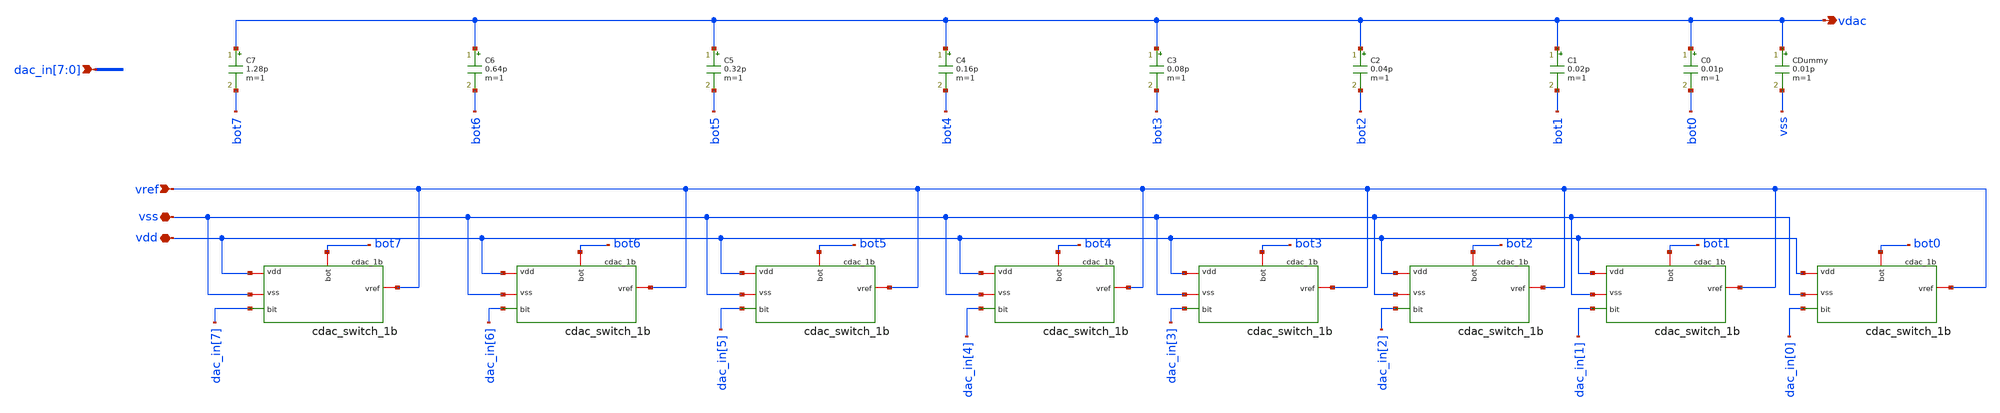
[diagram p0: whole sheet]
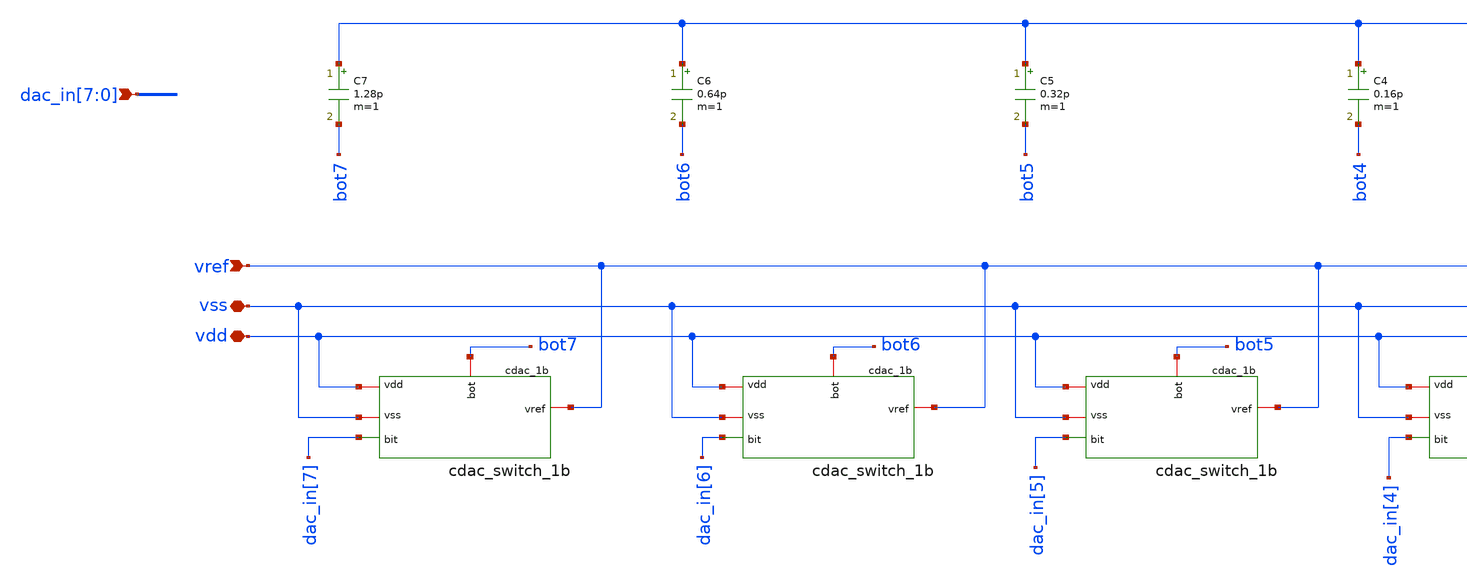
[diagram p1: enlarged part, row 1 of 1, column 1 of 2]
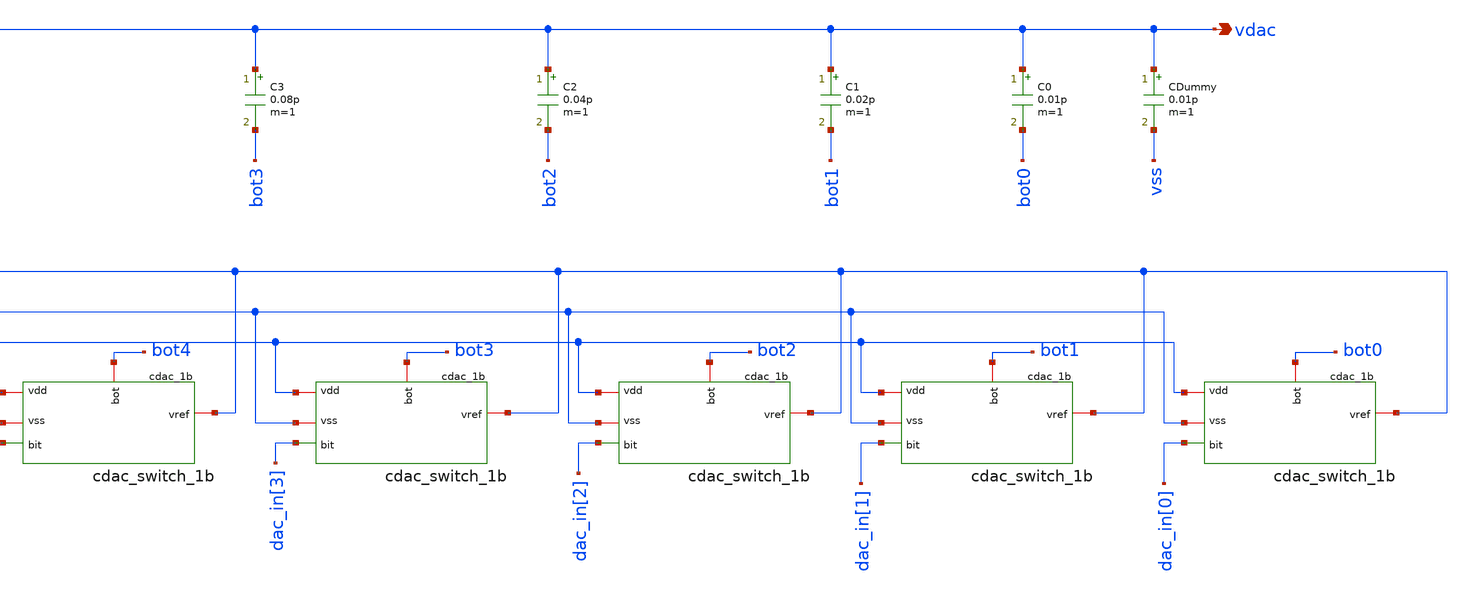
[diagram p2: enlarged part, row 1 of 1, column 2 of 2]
** sch_path: xschem/sar_adc/blocks/cdac/cdac_8bit.sch
**.subckt cdac_8bit vref vdd vss vdac
*+ dac_in[7],dac_in[6],dac_in[5],dac_in[4],dac_in[3],dac_in[2],dac_in[1],dac_in[0]
*.ipin vref
*.iopin vdd
*.iopin vss
*.opin vdac
*.ipin dac_in[7],dac_in[6],dac_in[5],dac_in[4],dac_in[3],dac_in[2],dac_in[1],dac_in[0]
C0 vdac bot0 0.01p m=1
C1 vdac bot1 0.02p m=1
C2 vdac bot2 0.04p m=1
C3 vdac bot3 0.08p m=1
C4 vdac bot4 0.16p m=1
C5 vdac bot5 0.32p m=1
C6 vdac bot6 0.64p m=1
C7 vdac bot7 1.28p m=1
XSW0 vref vdd vss bot0 dac_in[0] cdac_switch_1b
XSW1 vref vdd vss bot1 dac_in[1] cdac_switch_1b
XSW2 vref vdd vss bot2 dac_in[2] cdac_switch_1b
XSW3 vref vdd vss bot3 dac_in[3] cdac_switch_1b
XSW4 vref vdd vss bot4 dac_in[4] cdac_switch_1b
XSW5 vref vdd vss bot5 dac_in[5] cdac_switch_1b
XSW6 vref vdd vss bot6 dac_in[6] cdac_switch_1b
XSW7 vref vdd vss bot7 dac_in[7] cdac_switch_1b
CDummy vdac vss 0.01p m=1
**.ends

* expanding   symbol:  sar_adc/blocks/cdac/cdac_switch_1b.sym # of pins=5
** sym_path: xschem/sar_adc/blocks/cdac/cdac_switch_1b.sym
** sch_path: xschem/sar_adc/blocks/cdac/cdac_switch_1b.sch
.subckt cdac_switch_1b vref vdd vss bot bit
*.iopin vdd
*.iopin vss
*.iopin vref
*.ipin bit
*.iopin bot
XM1 bit_b bit vdd vdd pfet_03v3 L=0.28u W=1u nf=1 ad='int((nf+1)/2) * W/nf * 0.18u' as='int((nf+2)/2) * W/nf * 0.18u'
+ pd='2*int((nf+1)/2) * (W/nf + 0.18u)' ps='2*int((nf+2)/2) * (W/nf + 0.18u)' nrd='0.18u / W' nrs='0.18u / W'
+ sa=0 sb=0 sd=0 m=1
XM2 bit_b bit vss vss nfet_03v3 L=0.28u W=0.5u nf=1 ad='int((nf+1)/2) * W/nf * 0.18u' as='int((nf+2)/2) * W/nf * 0.18u'
+ pd='2*int((nf+1)/2) * (W/nf + 0.18u)' ps='2*int((nf+2)/2) * (W/nf + 0.18u)' nrd='0.18u / W' nrs='0.18u / W'
+ sa=0 sb=0 sd=0 m=1
XM3 bot bit_b vref vdd pfet_03v3 L=0.28u W=4u nf=1 ad='int((nf+1)/2) * W/nf * 0.18u' as='int((nf+2)/2) * W/nf * 0.18u'
+ pd='2*int((nf+1)/2) * (W/nf + 0.18u)' ps='2*int((nf+2)/2) * (W/nf + 0.18u)' nrd='0.18u / W' nrs='0.18u / W'
+ sa=0 sb=0 sd=0 m=1
XM4 vref bit bot vss nfet_03v3 L=0.28u W=2u nf=1 ad='int((nf+1)/2) * W/nf * 0.18u' as='int((nf+2)/2) * W/nf * 0.18u'
+ pd='2*int((nf+1)/2) * (W/nf + 0.18u)' ps='2*int((nf+2)/2) * (W/nf + 0.18u)' nrd='0.18u / W' nrs='0.18u / W'
+ sa=0 sb=0 sd=0 m=1
XM5 bot bit vss vdd pfet_03v3 L=0.28u W=4u nf=1 ad='int((nf+1)/2) * W/nf * 0.18u' as='int((nf+2)/2) * W/nf * 0.18u'
+ pd='2*int((nf+1)/2) * (W/nf + 0.18u)' ps='2*int((nf+2)/2) * (W/nf + 0.18u)' nrd='0.18u / W' nrs='0.18u / W'
+ sa=0 sb=0 sd=0 m=1
XM6 vss bit_b bot vss nfet_03v3 L=0.28u W=2u nf=1 ad='int((nf+1)/2) * W/nf * 0.18u' as='int((nf+2)/2) * W/nf * 0.18u'
+ pd='2*int((nf+1)/2) * (W/nf + 0.18u)' ps='2*int((nf+2)/2) * (W/nf + 0.18u)' nrd='0.18u / W' nrs='0.18u / W'
+ sa=0 sb=0 sd=0 m=1
.ends

.end
